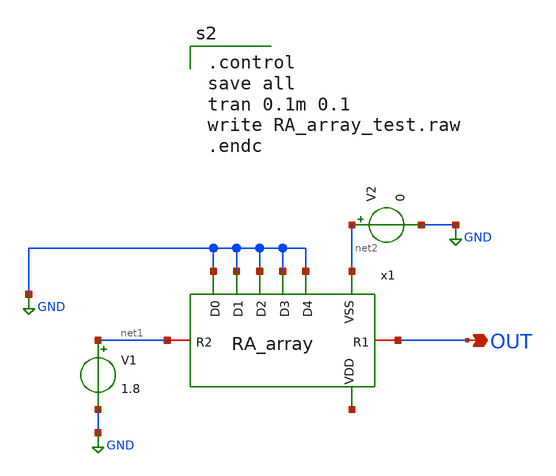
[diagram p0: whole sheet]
** sch_path: RA_array_test.sch
**.subckt RA_array_test OUT
*.opin OUT
x1 net2 OUT net1 GND GND GND GND GND net3 RA_array
V1 net1 GND 1.8
V2 net2 GND 0
**** begin user architecture code

.control
save all
tran 0.1m 0.1
write RA_array_test.raw
.endc


** opencircuitdesign pdks install
.lib $::SKYWATER_MODELS/sky130.lib.spice tt


**** end user architecture code
**.ends
.GLOBAL GND
.end
